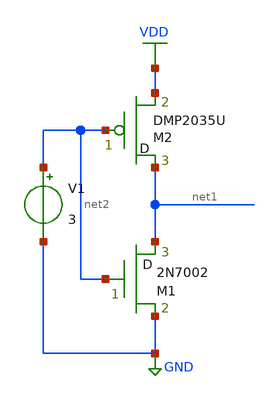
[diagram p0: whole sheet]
** sch_path: cmos.sch
**.subckt cmos
M1 net1 net2 GND M2N7002 m=1
M2 net1 net2 VDD DMP2035U m=1
V1 net2 GND 3
**** begin user architecture code
vout
**** end user architecture code
**.ends
.GLOBAL GND
.GLOBAL VDD
.end
